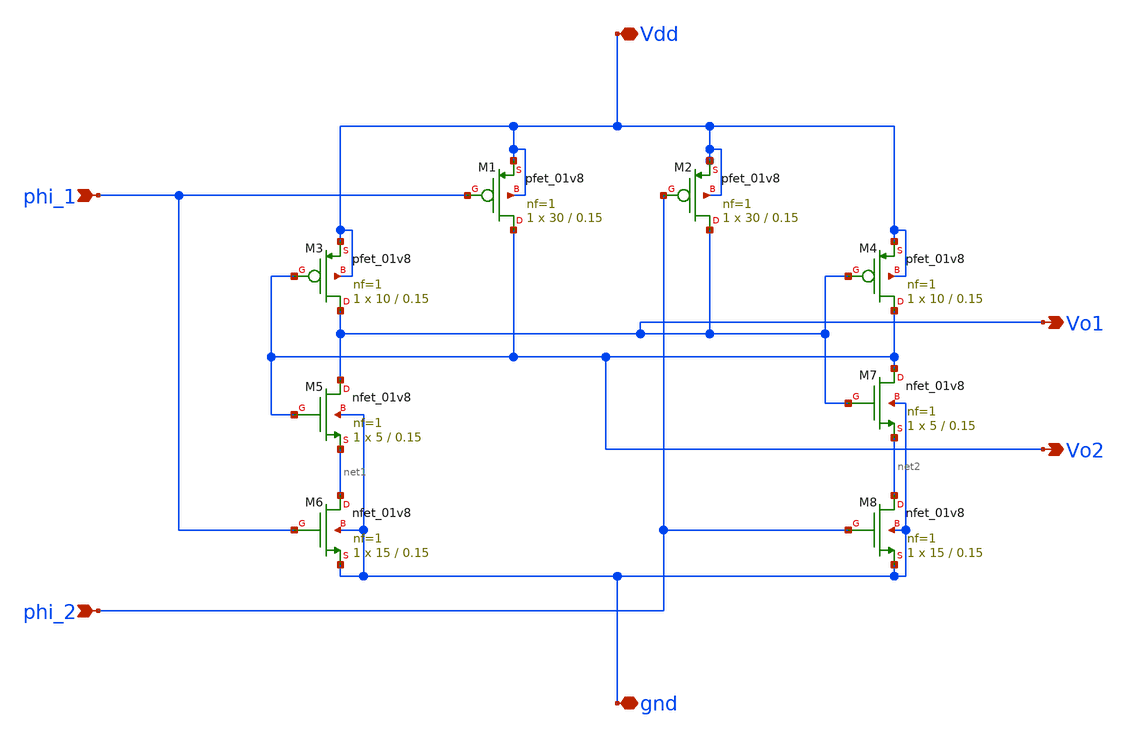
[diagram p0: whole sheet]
** sch_path: xschem/latch.sch
**.subckt latch phi_1 phi_2 Vdd gnd Vo1 Vo2
*.ipin phi_1
*.ipin phi_2
*.iopin Vdd
*.iopin gnd
*.opin Vo1
*.opin Vo2
XM1 Vo2 phi_1 Vdd Vdd sky130_fd_pr__pfet_01v8 L=0.15 W=30 nf=1 ad='int((nf+1)/2) * W/nf * 0.29' as='int((nf+2)/2) * W/nf * 0.29'
+ pd='2*int((nf+1)/2) * (W/nf + 0.29)' ps='2*int((nf+2)/2) * (W/nf + 0.29)' nrd='0.29 / W' nrs='0.29 / W'
+ sa=0 sb=0 sd=0 mult=1 m=1
XM2 Vo1 phi_2 Vdd Vdd sky130_fd_pr__pfet_01v8 L=0.15 W=30 nf=1 ad='int((nf+1)/2) * W/nf * 0.29' as='int((nf+2)/2) * W/nf * 0.29'
+ pd='2*int((nf+1)/2) * (W/nf + 0.29)' ps='2*int((nf+2)/2) * (W/nf + 0.29)' nrd='0.29 / W' nrs='0.29 / W'
+ sa=0 sb=0 sd=0 mult=1 m=1
XM3 Vo1 Vo2 Vdd Vdd sky130_fd_pr__pfet_01v8 L=0.15 W=10 nf=1 ad='int((nf+1)/2) * W/nf * 0.29' as='int((nf+2)/2) * W/nf * 0.29'
+ pd='2*int((nf+1)/2) * (W/nf + 0.29)' ps='2*int((nf+2)/2) * (W/nf + 0.29)' nrd='0.29 / W' nrs='0.29 / W'
+ sa=0 sb=0 sd=0 mult=1 m=1
XM4 Vo2 Vo1 Vdd Vdd sky130_fd_pr__pfet_01v8 L=0.15 W=10 nf=1 ad='int((nf+1)/2) * W/nf * 0.29' as='int((nf+2)/2) * W/nf * 0.29'
+ pd='2*int((nf+1)/2) * (W/nf + 0.29)' ps='2*int((nf+2)/2) * (W/nf + 0.29)' nrd='0.29 / W' nrs='0.29 / W'
+ sa=0 sb=0 sd=0 mult=1 m=1
XM5 Vo1 Vo2 net1 gnd sky130_fd_pr__nfet_01v8 L=0.15 W=5 nf=1 ad='int((nf+1)/2) * W/nf * 0.29' as='int((nf+2)/2) * W/nf * 0.29'
+ pd='2*int((nf+1)/2) * (W/nf + 0.29)' ps='2*int((nf+2)/2) * (W/nf + 0.29)' nrd='0.29 / W' nrs='0.29 / W'
+ sa=0 sb=0 sd=0 mult=1 m=1
XM6 net1 phi_1 gnd gnd sky130_fd_pr__nfet_01v8 L=0.15 W=15 nf=1 ad='int((nf+1)/2) * W/nf * 0.29' as='int((nf+2)/2) * W/nf * 0.29'
+ pd='2*int((nf+1)/2) * (W/nf + 0.29)' ps='2*int((nf+2)/2) * (W/nf + 0.29)' nrd='0.29 / W' nrs='0.29 / W'
+ sa=0 sb=0 sd=0 mult=1 m=1
XM7 Vo2 Vo1 net2 gnd sky130_fd_pr__nfet_01v8 L=0.15 W=5 nf=1 ad='int((nf+1)/2) * W/nf * 0.29' as='int((nf+2)/2) * W/nf * 0.29'
+ pd='2*int((nf+1)/2) * (W/nf + 0.29)' ps='2*int((nf+2)/2) * (W/nf + 0.29)' nrd='0.29 / W' nrs='0.29 / W'
+ sa=0 sb=0 sd=0 mult=1 m=1
XM8 net2 phi_2 gnd gnd sky130_fd_pr__nfet_01v8 L=0.15 W=15 nf=1 ad='int((nf+1)/2) * W/nf * 0.29' as='int((nf+2)/2) * W/nf * 0.29'
+ pd='2*int((nf+1)/2) * (W/nf + 0.29)' ps='2*int((nf+2)/2) * (W/nf + 0.29)' nrd='0.29 / W' nrs='0.29 / W'
+ sa=0 sb=0 sd=0 mult=1 m=1
**.ends
.end
